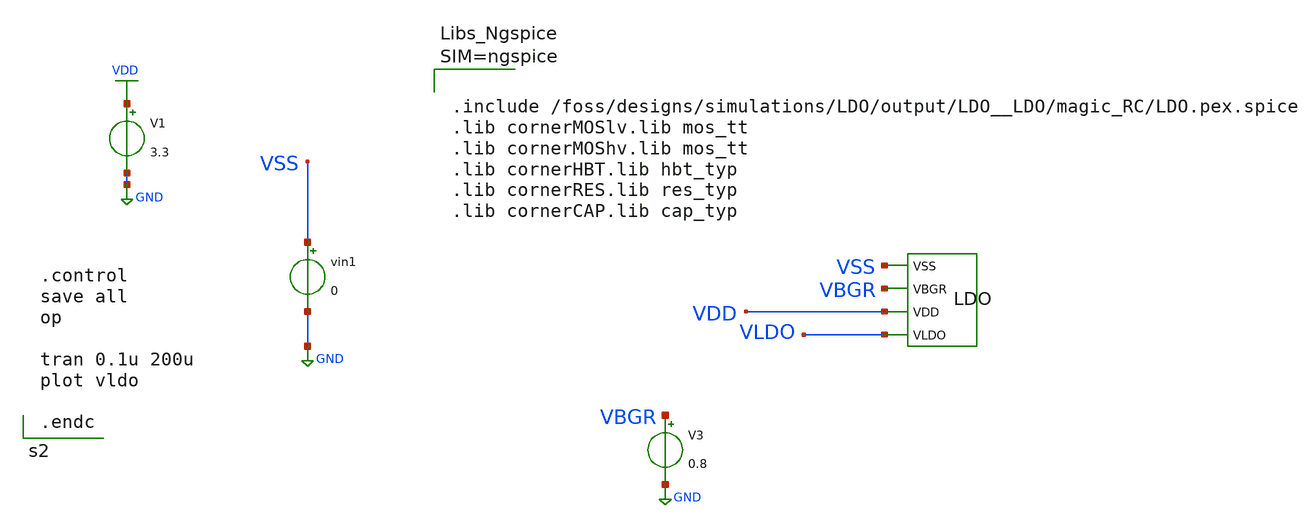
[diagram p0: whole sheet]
** sch_path: dependencies/LDO/LDO-main/testbenches/tran/xschem/ldo_post_layout_sim.sch
**.subckt ldo_post_layout_sim
V3 VBGR GND 0.8
vin1 VSS GND 0
X1 VSS VBGR VDD VLDO LDO
V1 VDD GND 3.3
**** begin user architecture code



.include /foss/designs/simulations/LDO/output/LDO__LDO/magic_RC/LDO.pex.spice
.lib cornerMOSlv.lib mos_tt
.lib cornerMOShv.lib mos_tt
.lib cornerHBT.lib hbt_typ
.lib cornerRES.lib res_typ
.lib cornerCAP.lib cap_typ





.control
save all
op

tran 0.1u 200u
plot vldo

.endc

**** end user architecture code
**.ends
.GLOBAL GND
.GLOBAL VDD
.end
